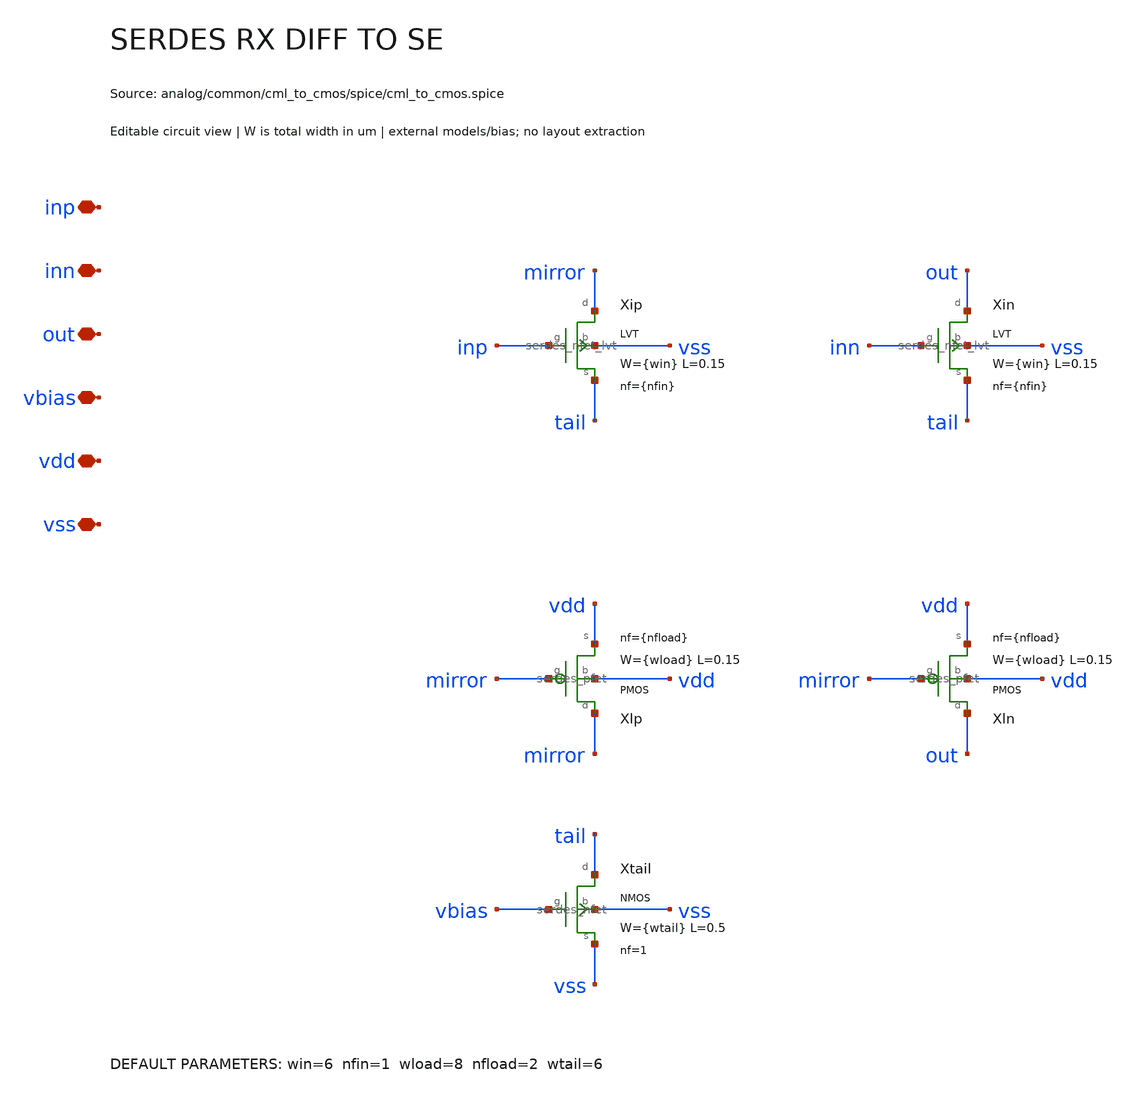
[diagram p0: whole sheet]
** sch_path: analog/common/cml_to_cmos/schematic/serdes_rx_diff_to_se.sch
**.subckt serdes_rx_diff_to_se inp inn out vbias vdd vss
*.iopin inp
*.iopin inn
*.iopin out
*.iopin vbias
*.iopin vdd
*.iopin vss
Xip mirror inp tail vss serdes_nfet_lvt w={win} l=0.15 nf={nfin}
Xin out inn tail vss serdes_nfet_lvt w={win} l=0.15 nf={nfin}
Xlp mirror mirror vdd vdd serdes_pfet w={wload} l=0.15 nf={nfload}
Xln out mirror vdd vdd serdes_pfet w={wload} l=0.15 nf={nfload}
Xtail tail vbias vss vss serdes_nfet w={wtail} l=0.5 nf=1
**.ends

* expanding   symbol:  serdes/serdes_nfet_lvt.sym # of pins=4
** sym_path: analog/common/devices/schematic/serdes_nfet_lvt.sym
** sch_path: analog/common/devices/schematic/serdes_nfet_lvt.sch
.subckt serdes_nfet_lvt d g s b  w=1 l=0.15 nf=1
*.iopin d
*.iopin g
*.iopin s
*.iopin b
Xmos d g s b sky130_fd_pr__nfet_01v8_lvt w={w} l={l} nf={nf} ad={floor((nf+1)/2)*(w/nf)*0.29} as={floor((nf+2)/2)*(w/nf)*0.29}
+ pd={2*floor((nf+1)/2)*(w/nf+0.29)} ps={2*floor((nf+2)/2)*(w/nf+0.29)}
.ends


* expanding   symbol:  serdes/serdes_pfet.sym # of pins=4
** sym_path: analog/common/devices/schematic/serdes_pfet.sym
** sch_path: analog/common/devices/schematic/serdes_pfet.sch
.subckt serdes_pfet d g s b  w=3 l=0.15 nf=1
*.iopin d
*.iopin g
*.iopin s
*.iopin b
Xmos d g s b sky130_fd_pr__pfet_01v8 w={w} l={l} nf={nf} ad={floor((nf+1)/2)*(w/nf)*0.29} as={floor((nf+2)/2)*(w/nf)*0.29}
+ pd={2*floor((nf+1)/2)*(w/nf+0.29)} ps={2*floor((nf+2)/2)*(w/nf+0.29)}
.ends


* expanding   symbol:  serdes/serdes_nfet.sym # of pins=4
** sym_path: analog/common/devices/schematic/serdes_nfet.sym
** sch_path: analog/common/devices/schematic/serdes_nfet.sch
.subckt serdes_nfet d g s b  w=1 l=0.15 nf=1
*.iopin d
*.iopin g
*.iopin s
*.iopin b
Xmos d g s b sky130_fd_pr__nfet_01v8 w={w} l={l} nf={nf} ad={floor((nf+1)/2)*(w/nf)*0.29} as={floor((nf+2)/2)*(w/nf)*0.29}
+ pd={2*floor((nf+1)/2)*(w/nf+0.29)} ps={2*floor((nf+2)/2)*(w/nf+0.29)}
.ends

.end
